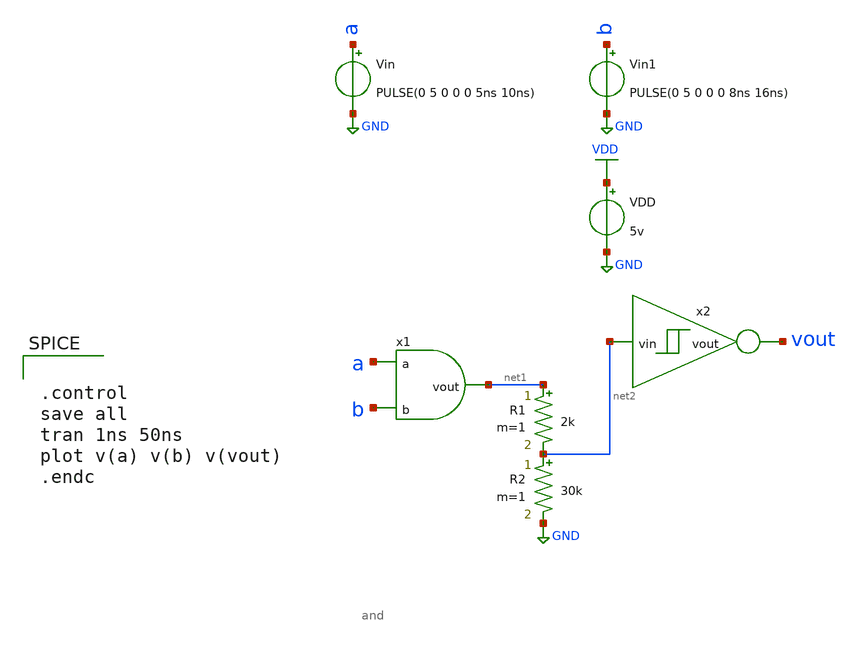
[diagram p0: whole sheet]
** sch_path: schematics/and_tb.sch
**.subckt and_tb
Vin a GND PULSE(0 5 0 0 0 5ns 10ns)
VDD VDD GND 5v
x1 net1 a b and
Vin1 b GND PULSE(0 5 0 0 0 8ns 16ns)
x2 vout net2 schmitt_trigger
R1 net1 net2 2k m=1
R2 net2 GND 30k m=1
**** begin user architecture code


.control
save all
tran 1ns 50ns
plot v(a) v(b) v(vout)
.endc


 .lib $::SKYWATER_MODELS/models/sky130.lib.spice tt

.param mc_mm_switch=0
.param mc_pr_switch=1

**** end user architecture code
**.ends

* expanding   symbol:  /media/sf_share/final_project/and.sym # of pins=3
** sym_path: schematics/and.sym
** sch_path: schematics/and.sch
.subckt and vout a b
*.ipin a
*.opin vout
*.ipin b
XM1 net1 b GND GND sky130_fd_pr__nfet_g5v0d10v5 L=0.5 W=0.5 nf=1 ad='int((nf+1)/2) * W/nf * 0.29' as='int((nf+2)/2) * W/nf * 0.29'
+ pd='2*int((nf+1)/2) * (W/nf + 0.29)' ps='2*int((nf+2)/2) * (W/nf + 0.29)' nrd='0.29 / W' nrs='0.29 / W'
+ sa=0 sb=0 sd=0 mult=1 m=1
XM5 net2 a net1 GND sky130_fd_pr__nfet_g5v0d10v5 L=0.5 W=0.5 nf=1 ad='int((nf+1)/2) * W/nf * 0.29' as='int((nf+2)/2) * W/nf * 0.29'
+ pd='2*int((nf+1)/2) * (W/nf + 0.29)' ps='2*int((nf+2)/2) * (W/nf + 0.29)' nrd='0.29 / W' nrs='0.29 / W'
+ sa=0 sb=0 sd=0 mult=1 m=1
XM2 net2 a VDD VDD sky130_fd_pr__pfet_g5v0d10v5 L=0.5 W=0.5 nf=1 ad='int((nf+1)/2) * W/nf * 0.29' as='int((nf+2)/2) * W/nf * 0.29'
+ pd='2*int((nf+1)/2) * (W/nf + 0.29)' ps='2*int((nf+2)/2) * (W/nf + 0.29)' nrd='0.29 / W' nrs='0.29 / W'
+ sa=0 sb=0 sd=0 mult=1 m=1
XM4 net2 b VDD VDD sky130_fd_pr__pfet_g5v0d10v5 L=0.5 W=0.5 nf=1 ad='int((nf+1)/2) * W/nf * 0.29' as='int((nf+2)/2) * W/nf * 0.29'
+ pd='2*int((nf+1)/2) * (W/nf + 0.29)' ps='2*int((nf+2)/2) * (W/nf + 0.29)' nrd='0.29 / W' nrs='0.29 / W'
+ sa=0 sb=0 sd=0 mult=1 m=1
x1 vout net2 inverter
.ends


* expanding   symbol:  /media/sf_share/final_project/schmitt_trigger.sym # of pins=2
** sym_path: schematics/schmitt_trigger.sym
** sch_path: schematics/schmitt_trigger.sch
.subckt schmitt_trigger vout vin
*.ipin vin
*.opin vout
XM1 net1 vin net3 GND sky130_fd_pr__nfet_g5v0d10v5 L=1 W=15 nf=1 ad='int((nf+1)/2) * W/nf * 0.29' as='int((nf+2)/2) * W/nf * 0.29'
+ pd='2*int((nf+1)/2) * (W/nf + 0.29)' ps='2*int((nf+2)/2) * (W/nf + 0.29)' nrd='0.29 / W' nrs='0.29 / W'
+ sa=0 sb=0 sd=0 mult=1 m=1
XM2 net1 vin net2 VDD sky130_fd_pr__pfet_g5v0d10v5 L=1 W=15 nf=1 ad='int((nf+1)/2) * W/nf * 0.29' as='int((nf+2)/2) * W/nf * 0.29'
+ pd='2*int((nf+1)/2) * (W/nf + 0.29)' ps='2*int((nf+2)/2) * (W/nf + 0.29)' nrd='0.29 / W' nrs='0.29 / W'
+ sa=0 sb=0 sd=0 mult=1 m=1
XM3 net2 vin VDD VDD sky130_fd_pr__pfet_g5v0d10v5 L=1 W=1.5 nf=1 ad='int((nf+1)/2) * W/nf * 0.29' as='int((nf+2)/2) * W/nf * 0.29'
+ pd='2*int((nf+1)/2) * (W/nf + 0.29)' ps='2*int((nf+2)/2) * (W/nf + 0.29)' nrd='0.29 / W' nrs='0.29 / W'
+ sa=0 sb=0 sd=0 mult=1 m=1
XM4 net3 vin GND GND sky130_fd_pr__nfet_g5v0d10v5 L=1 W=1.05 nf=1 ad='int((nf+1)/2) * W/nf * 0.29' as='int((nf+2)/2) * W/nf * 0.29'
+ pd='2*int((nf+1)/2) * (W/nf + 0.29)' ps='2*int((nf+2)/2) * (W/nf + 0.29)' nrd='0.29 / W' nrs='0.29 / W'
+ sa=0 sb=0 sd=0 mult=1 m=1
XM5 GND net1 net2 VDD sky130_fd_pr__pfet_g5v0d10v5 L=15 W=1 nf=1 ad='int((nf+1)/2) * W/nf * 0.29' as='int((nf+2)/2) * W/nf * 0.29'
+ pd='2*int((nf+1)/2) * (W/nf + 0.29)' ps='2*int((nf+2)/2) * (W/nf + 0.29)' nrd='0.29 / W' nrs='0.29 / W'
+ sa=0 sb=0 sd=0 mult=1 m=1
XM6 VDD net1 net3 GND sky130_fd_pr__nfet_g5v0d10v5 L=5.5 W=1 nf=1 ad='int((nf+1)/2) * W/nf * 0.29' as='int((nf+2)/2) * W/nf * 0.29'
+ pd='2*int((nf+1)/2) * (W/nf + 0.29)' ps='2*int((nf+2)/2) * (W/nf + 0.29)' nrd='0.29 / W' nrs='0.29 / W'
+ sa=0 sb=0 sd=0 mult=1 m=1
x1 vout net1 inverter
.ends


* expanding   symbol:  /media/sf_share/final_project/inverter.sym # of pins=2
** sym_path: schematics/inverter.sym
** sch_path: schematics/inverter.sch
.subckt inverter vout vin
*.ipin vin
*.opin vout
XM3 vout vin VDD VDD sky130_fd_pr__pfet_g5v0d10v5 L=0.5 W=0.5 nf=1 ad='int((nf+1)/2) * W/nf * 0.29' as='int((nf+2)/2) * W/nf * 0.29'
+ pd='2*int((nf+1)/2) * (W/nf + 0.29)' ps='2*int((nf+2)/2) * (W/nf + 0.29)' nrd='0.29 / W' nrs='0.29 / W'
+ sa=0 sb=0 sd=0 mult=1 m=1
XM5 vout vin GND GND sky130_fd_pr__nfet_g5v0d10v5 L=0.5 W=0.5 nf=1 ad='int((nf+1)/2) * W/nf * 0.29' as='int((nf+2)/2) * W/nf * 0.29'
+ pd='2*int((nf+1)/2) * (W/nf + 0.29)' ps='2*int((nf+2)/2) * (W/nf + 0.29)' nrd='0.29 / W' nrs='0.29 / W'
+ sa=0 sb=0 sd=0 mult=1 m=1
.ends

.GLOBAL VDD
.GLOBAL GND
.end
